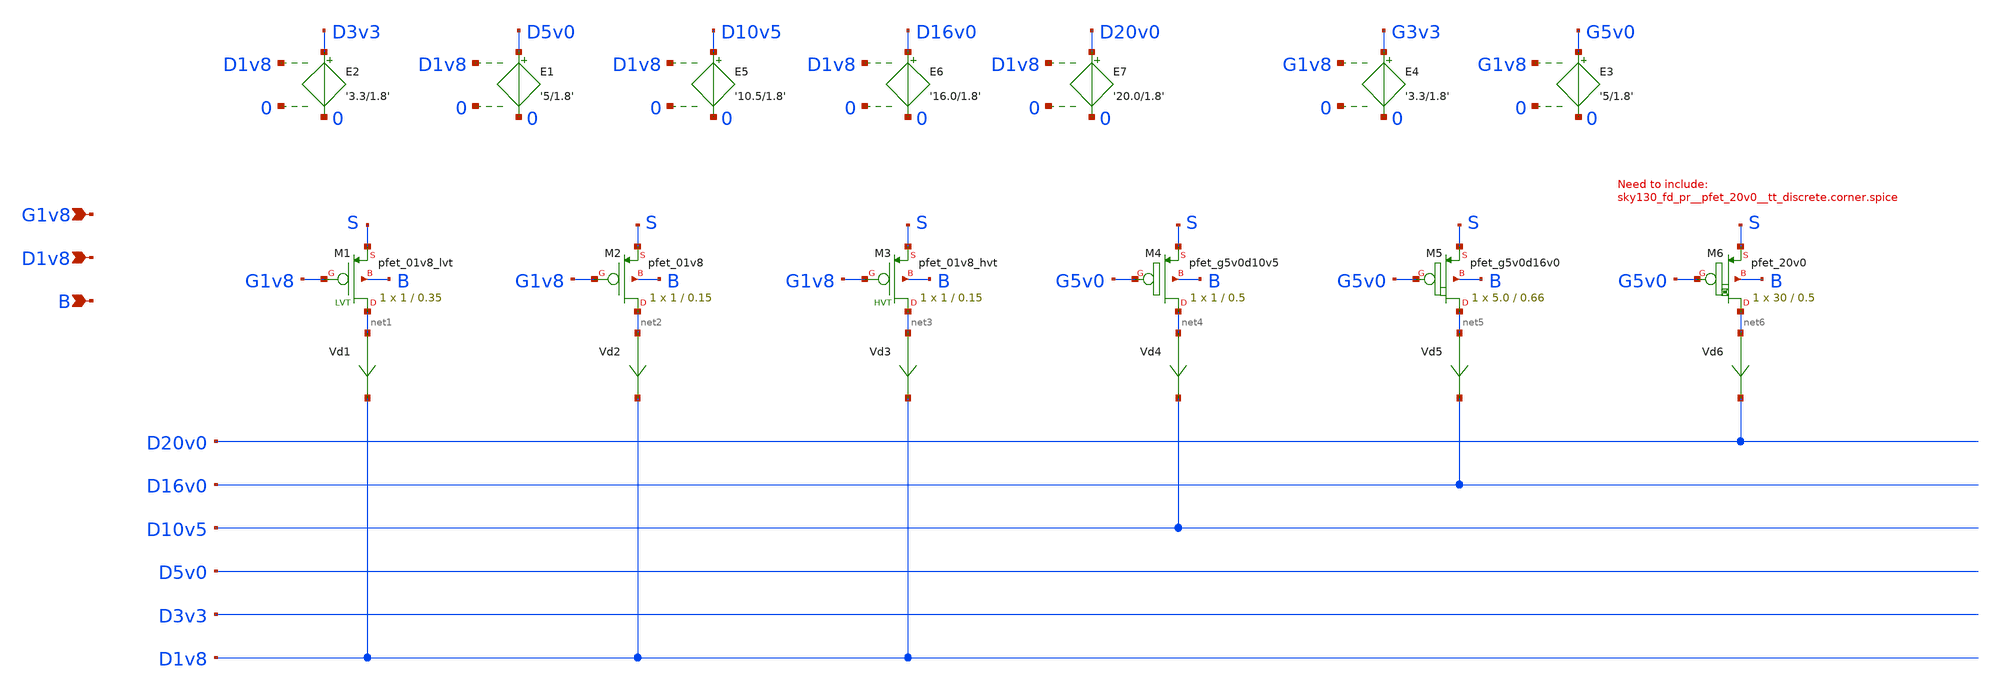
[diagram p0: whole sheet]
** sch_path: xyce/sky130A-xyce/libs.tech/xschem/sky130_tests/test_pmos.sch
* Copyright 2020 Stefan Frederik Schippers
* Licensed under the Apache License, Version 2.0 (the "License");
* you may not use this file except in compliance with the License.
* You may obtain a copy of the License at
* https://www.apache.org/licenses/LICENSE-2.0
* Unless required by applicable law or agreed to in writing, software
* distributed under the License is distributed on an "AS IS" BASIS,
* WITHOUT WARRANTIES OR CONDITIONS OF ANY KIND, either express or implied.
* See the License for the specific language governing permissions and
* limitations under the License.
**.subckt test_pmos G1v8 D1v8 B
*.ipin G1v8
*.ipin D1v8
*.ipin B
Vd1 net1 D1v8 0
.save i(vd1)
Vd2 net2 D1v8 0
.save i(vd2)
E1 D5v0 0 D1v8 0 '5/1.8'
E2 D3v3 0 D1v8 0 '3.3/1.8'
E3 G5v0 0 G1v8 0 '5/1.8'
E4 G3v3 0 G1v8 0 '3.3/1.8'
E5 D10v5 0 D1v8 0 '10.5/1.8'
Vd3 net3 D1v8 0
.save i(vd3)
XM3 net3 G1v8 S B sky130_fd_pr__pfet_01v8_hvt L=0.15 W=1 nf=1 ad='int((nf+1)/2) * W/nf * 0.29' as='int((nf+2)/2) * W/nf * 0.29'
+ pd='2*int((nf+1)/2) * (W/nf + 0.29)' ps='2*int((nf+2)/2) * (W/nf + 0.29)' nrd='0.29 / W' nrs='0.29 / W'
+ sa=0 sb=0 sd=0 mult=1 m=1
Vd4 net4 D10v5 0
.save i(vd4)
XM4 net4 G5v0 S B sky130_fd_pr__pfet_g5v0d10v5 L=0.5 W=1 nf=1 ad='int((nf+1)/2) * W/nf * 0.29' as='int((nf+2)/2) * W/nf * 0.29'
+ pd='2*int((nf+1)/2) * (W/nf + 0.29)' ps='2*int((nf+2)/2) * (W/nf + 0.29)' nrd='0.29 / W' nrs='0.29 / W'
+ sa=0 sb=0 sd=0 mult=1 m=1
XM1 net1 G1v8 S B sky130_fd_pr__pfet_01v8_lvt L=0.35 W=1 nf=1 ad='int((nf+1)/2) * W/nf * 0.29' as='int((nf+2)/2) * W/nf * 0.29'
+ pd='2*int((nf+1)/2) * (W/nf + 0.29)' ps='2*int((nf+2)/2) * (W/nf + 0.29)' nrd='0.29 / W' nrs='0.29 / W'
+ sa=0 sb=0 sd=0 mult=1 m=1
XM2 net2 G1v8 S B sky130_fd_pr__pfet_01v8 L=0.15 W=1 nf=1 ad='int((nf+1)/2) * W/nf * 0.29' as='int((nf+2)/2) * W/nf * 0.29'
+ pd='2*int((nf+1)/2) * (W/nf + 0.29)' ps='2*int((nf+2)/2) * (W/nf + 0.29)' nrd='0.29 / W' nrs='0.29 / W'
+ sa=0 sb=0 sd=0 mult=1 m=1
Vd5 net5 D16v0 0
.save i(vd5)
XM5 net5 G5v0 S B sky130_fd_pr__pfet_g5v0d16v0 L=0.66 W=5.0 nf=1 ad='int((nf+1)/2) * W/nf * 0.29' as='int((nf+2)/2) * W/nf * 0.29'
+ pd='2*int((nf+1)/2) * (W/nf + 0.29)' ps='2*int((nf+2)/2) * (W/nf + 0.29)' nrd='0.29 / W' nrs='0.29 / W'
+ sa=0 sb=0 sd=0 mult=1 m=1
E6 D16v0 0 D1v8 0 '16.0/1.8'
E7 D20v0 0 D1v8 0 '20.0/1.8'
XM6 net6 G5v0 S B sky130_fd_pr__pfet_20v0 L=0.5 W=30 m=1
Vd6 net6 D20v0 0
.save i(vd6)
**** begin user architecture code


vg G1v8 0 0
vs s 0 0
vd D1v8 0 0
vb b 0 0
.control
save all
dc vd 0 -1.8 -0.01 vg 0 -1.8 -0.2
plot all.vd1#branch vs D1v8
plot all.vd2#branch vs D1v8
plot all.vd3#branch vs D1v8
plot all.vd4#branch vs D10v5
plot all.vd5#branch vs D16v0
plot all.vd6#branch vs D20v0
.endc



.include $::SKYWATER_MODELS/cells/nfet_01v8/sky130_fd_pr__nfet_01v8__tt.corner.spice
.include $::SKYWATER_MODELS/cells/nfet_01v8_lvt/sky130_fd_pr__nfet_01v8_lvt__tt.corner.spice
.include $::SKYWATER_MODELS/cells/pfet_01v8/sky130_fd_pr__pfet_01v8__tt.corner.spice
.include $::SKYWATER_MODELS/cells/nfet_03v3_nvt/sky130_fd_pr__nfet_03v3_nvt__tt.corner.spice
.include $::SKYWATER_MODELS/cells/nfet_05v0_nvt/sky130_fd_pr__nfet_05v0_nvt__tt.corner.spice
.include $::SKYWATER_MODELS/cells/esd_nfet_01v8/sky130_fd_pr__esd_nfet_01v8__tt.corner.spice
.include $::SKYWATER_MODELS/cells/pfet_01v8_lvt/sky130_fd_pr__pfet_01v8_lvt__tt.corner.spice
.include $::SKYWATER_MODELS/cells/pfet_01v8_hvt/sky130_fd_pr__pfet_01v8_hvt__tt.corner.spice
.include $::SKYWATER_MODELS/cells/esd_pfet_g5v0d10v5/sky130_fd_pr__esd_pfet_g5v0d10v5__tt.corner.spice
.include $::SKYWATER_MODELS/cells/pfet_g5v0d10v5/sky130_fd_pr__pfet_g5v0d10v5__tt.corner.spice
.include $::SKYWATER_MODELS/cells/pfet_g5v0d16v0/sky130_fd_pr__pfet_g5v0d16v0__tt.corner.spice
.include $::SKYWATER_MODELS/cells/nfet_g5v0d10v5/sky130_fd_pr__nfet_g5v0d10v5__tt.corner.spice
.include $::SKYWATER_MODELS/cells/nfet_g5v0d16v0/sky130_fd_pr__nfet_g5v0d16v0__tt_discrete.corner.spice
.include $::SKYWATER_MODELS/cells/esd_nfet_g5v0d10v5/sky130_fd_pr__esd_nfet_g5v0d10v5__tt.corner.spice
.include $::SKYWATER_MODELS/models/corners/tt/nonfet.spice
* Mismatch parameters
.include $::SKYWATER_MODELS/cells/nfet_01v8/sky130_fd_pr__nfet_01v8__mismatch.corner.spice
.include $::SKYWATER_MODELS/cells/pfet_01v8/sky130_fd_pr__pfet_01v8__mismatch.corner.spice
.include $::SKYWATER_MODELS/cells/nfet_01v8_lvt/sky130_fd_pr__nfet_01v8_lvt__mismatch.corner.spice
.include $::SKYWATER_MODELS/cells/pfet_01v8_lvt/sky130_fd_pr__pfet_01v8_lvt__mismatch.corner.spice
.include $::SKYWATER_MODELS/cells/pfet_01v8_hvt/sky130_fd_pr__pfet_01v8_hvt__mismatch.corner.spice
.include $::SKYWATER_MODELS/cells/nfet_g5v0d10v5/sky130_fd_pr__nfet_g5v0d10v5__mismatch.corner.spice
.include $::SKYWATER_MODELS/cells/pfet_g5v0d10v5/sky130_fd_pr__pfet_g5v0d10v5__mismatch.corner.spice
.include $::SKYWATER_MODELS/cells/nfet_05v0_nvt/sky130_fd_pr__nfet_05v0_nvt__mismatch.corner.spice
.include $::SKYWATER_MODELS/cells/nfet_03v3_nvt/sky130_fd_pr__nfet_03v3_nvt__mismatch.corner.spice
* Resistor$::SKYWATER_MODELS/Capacitor
.include $::SKYWATER_MODELS/models/r+c/res_typical__cap_typical.spice
.include $::SKYWATER_MODELS/models/r+c/res_typical__cap_typical__lin.spice
* Special cells
.include $::SKYWATER_MODELS/models/corners/tt/specialized_cells.spice
* All models
.include $::SKYWATER_MODELS/models/all.spice
* Corner
.include $::SKYWATER_MODELS/models/corners/tt/rf.spice


.include $::SKYWATER_MODELS/cells/pfet_20v0/sky130_fd_pr__pfet_20v0__tt_discrete.corner.spice

**** end user architecture code
**.ends
.end
